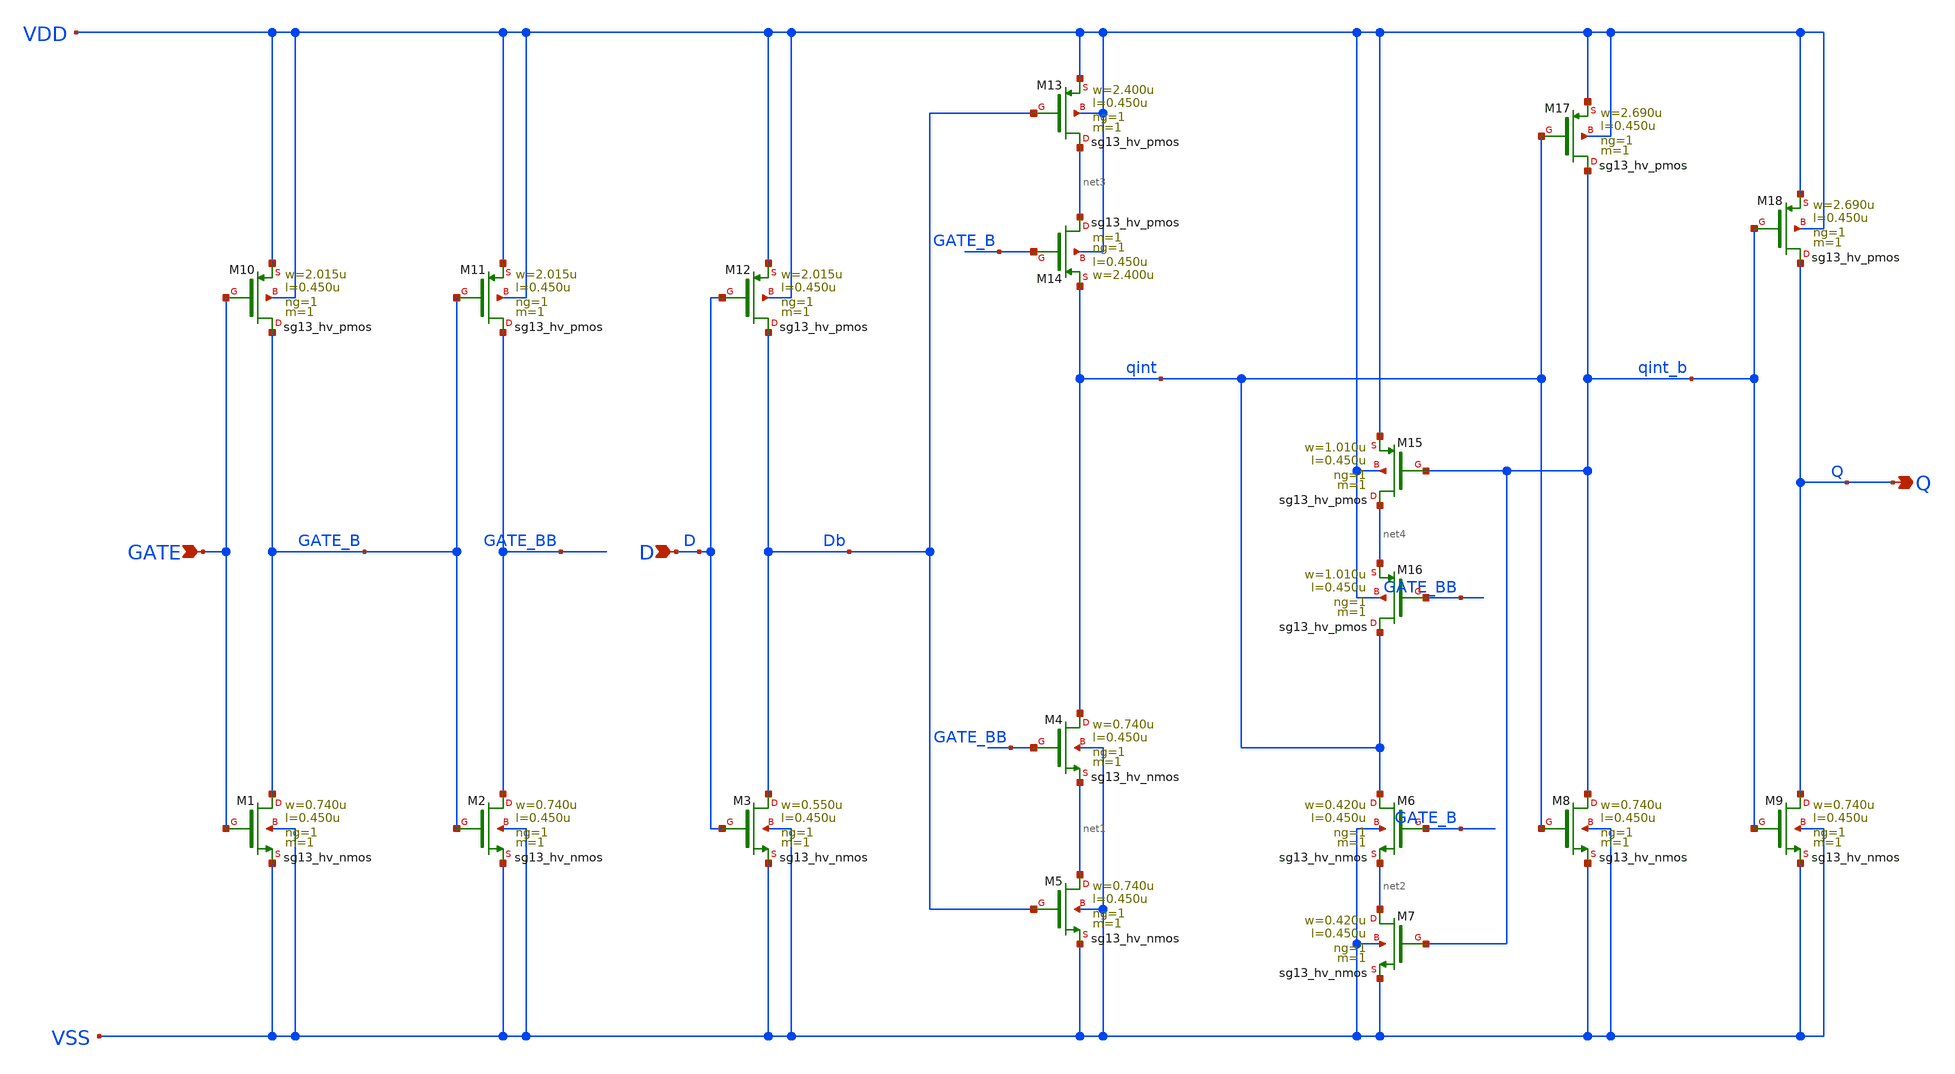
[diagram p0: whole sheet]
** sch_path: ihp-sg13g2/libs.ref/sg13g2_stdcell_hv/sch/xschem/sg13g2_hv_dlhq_1.sch
* Copyright 2023 IHP PDK Authors
* Licensed under the Apache License, Version 2.0 (the "License");
* you may not use this file except in compliance with the License.
* You may obtain a copy of the License at
* https://www.apache.org/licenses/LICENSE-2.0
* Unless required by applicable law or agreed to in writing, software
* distributed under the License is distributed on an "AS IS" BASIS,
* WITHOUT WARRANTIES OR CONDITIONS OF ANY KIND, either express or implied.
* See the License for the specific language governing permissions and
* limitations under the License.
**.subckt sg13g2_hv_dlhq_1 Q GATE D
*.opin Q
*.ipin GATE
*.ipin D
XM1 GATE_B GATE VSS VSS sg13_hv_nmos w=0.740u l=0.450u ng=1 m=1 mm_ok=1
XM2 GATE_BB GATE_B VSS VSS sg13_hv_nmos w=0.740u l=0.450u ng=1 m=1 mm_ok=1
XM3 Db D VSS VSS sg13_hv_nmos w=0.550u l=0.450u ng=1 m=1 mm_ok=1
XM4 qint GATE_BB net1 VSS sg13_hv_nmos w=0.740u l=0.450u ng=1 m=1 mm_ok=1
XM5 net1 Db VSS VSS sg13_hv_nmos w=0.740u l=0.450u ng=1 m=1 mm_ok=1
XM6 qint GATE_B net2 VSS sg13_hv_nmos w=0.420u l=0.450u ng=1 m=1 mm_ok=1
XM7 net2 qint_b VSS VSS sg13_hv_nmos w=0.420u l=0.450u ng=1 m=1 mm_ok=1
XM8 qint_b qint VSS VSS sg13_hv_nmos w=0.740u l=0.450u ng=1 m=1 mm_ok=1
XM9 Q qint_b VSS VSS sg13_hv_nmos w=0.740u l=0.450u ng=1 m=1 mm_ok=1
XM10 GATE_B GATE VDD VDD sg13_hv_pmos w=2.015u l=0.450u ng=1 m=1 mm_ok=1
XM11 GATE_BB GATE_B VDD VDD sg13_hv_pmos w=2.015u l=0.450u ng=1 m=1 mm_ok=1
XM12 Db D VDD VDD sg13_hv_pmos w=2.015u l=0.450u ng=1 m=1 mm_ok=1
XM13 net3 Db VDD VDD sg13_hv_pmos w=2.400u l=0.450u ng=1 m=1 mm_ok=1
XM14 net3 GATE_B qint VDD sg13_hv_pmos w=2.400u l=0.450u ng=1 m=1 mm_ok=1
XM15 net4 qint_b VDD VDD sg13_hv_pmos w=1.010u l=0.450u ng=1 m=1 mm_ok=1
XM16 qint GATE_BB net4 VDD sg13_hv_pmos w=1.010u l=0.450u ng=1 m=1 mm_ok=1
XM17 qint_b qint VDD VDD sg13_hv_pmos w=2.690u l=0.450u ng=1 m=1 mm_ok=1
XM18 Q qint_b VDD VDD sg13_hv_pmos w=2.690u l=0.450u ng=1 m=1 mm_ok=1
**.ends
.end
